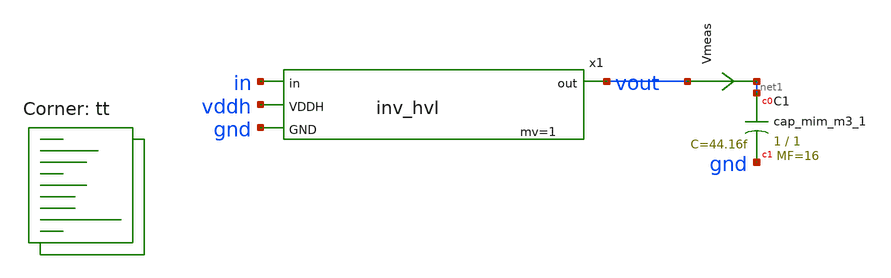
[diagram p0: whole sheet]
** sch_path: xschem/inv_hvl-tb.sch
**.subckt inv_hvl-tb
XC1 net1 gnd sky130_fd_pr__cap_mim_m3_1 W=1 L=1 MF=16 m=16
x1 in vout vddh gnd inv_hvl mv=1
Vmeas vout net1 0
.save i(vmeas)
**** begin user architecture code
.lib $::SKYWATER_MODELS/sky130.lib.spice tt



  .option wnflag=1
  .option safecurrents
  ********************Static Voltage Sources***************************
  Vddh vddh gnd dc 5.5

  ********************Dynamic Voltage Sources***************************
  *******Calculation**********
  .param base_f=100e3 base_t={1/base_f} base_th={base_t/2} base_d={base_th}
  .param d2_th ={base_th} d2_t={2*d2_th}
  .param d1_th ={4*d2_th} d1_t={d0_th}
  .param d0_th ={4*d1_th} d0_t={4*d0_th}

  .param d20_d ={0} d21_d={1*d2_th} d22_d={2*d2_th} d23_d={3*d2_th}
  .param d10_d ={0} d11_d={1*d1_th} d12_d={2*d1_th} d13_d={3*d1_th}
  .param d00_d ={0} d01_d={1*d0_th} d02_d={2*d0_th} d03_d={3*d0_th}
  *******Signals**********
  .param vhi=5.5
  Vin in gnd pulse(0 {vhi} {0} 1p 1p {10u} {20u})
  ********************Simulation Commands*****************************
  .control
     reset
     save all
     tran 1n 50u
     write inv_hvl-tb.raw
     set appendwrite

     reset
     save all
     dc vin 0 5.5 0.1
     write inv_hvl-tb.raw
*    quit 0
  .endc



**** end user architecture code
**.ends

* expanding   symbol:  inv_hvl.sym # of pins=4
** sym_path: xschem/inv_hvl.sym
** sch_path: xschem/inv_hvl.sch
.subckt inv_hvl in out VDDH GND  mv=1
*.opin out
*.ipin VDDH
*.ipin GND
*.ipin in
.param wp=0.84 wn=0.42 l=0.5
XM1 out in VDDH VDDH sky130_fd_pr__pfet_g5v0d10v5 L=l W=wp nf=1 ad='int((nf+1)/2) * W/nf * 0.29' as='int((nf+2)/2) * W/nf * 0.29'
+ pd='2*int((nf+1)/2) * (W/nf + 0.29)' ps='2*int((nf+2)/2) * (W/nf + 0.29)' nrd='0.29 / W' nrs='0.29 / W'
+ sa=0 sb=0 sd=0 mult=mv m=mv
XM2 out in GND GND sky130_fd_pr__nfet_g5v0d10v5 L=l W=wn nf=1 ad='int((nf+1)/2) * W/nf * 0.29' as='int((nf+2)/2) * W/nf * 0.29'
+ pd='2*int((nf+1)/2) * (W/nf + 0.29)' ps='2*int((nf+2)/2) * (W/nf + 0.29)' nrd='0.29 / W' nrs='0.29 / W'
+ sa=0 sb=0 sd=0 mult=mv m=mv
.ends

.end
